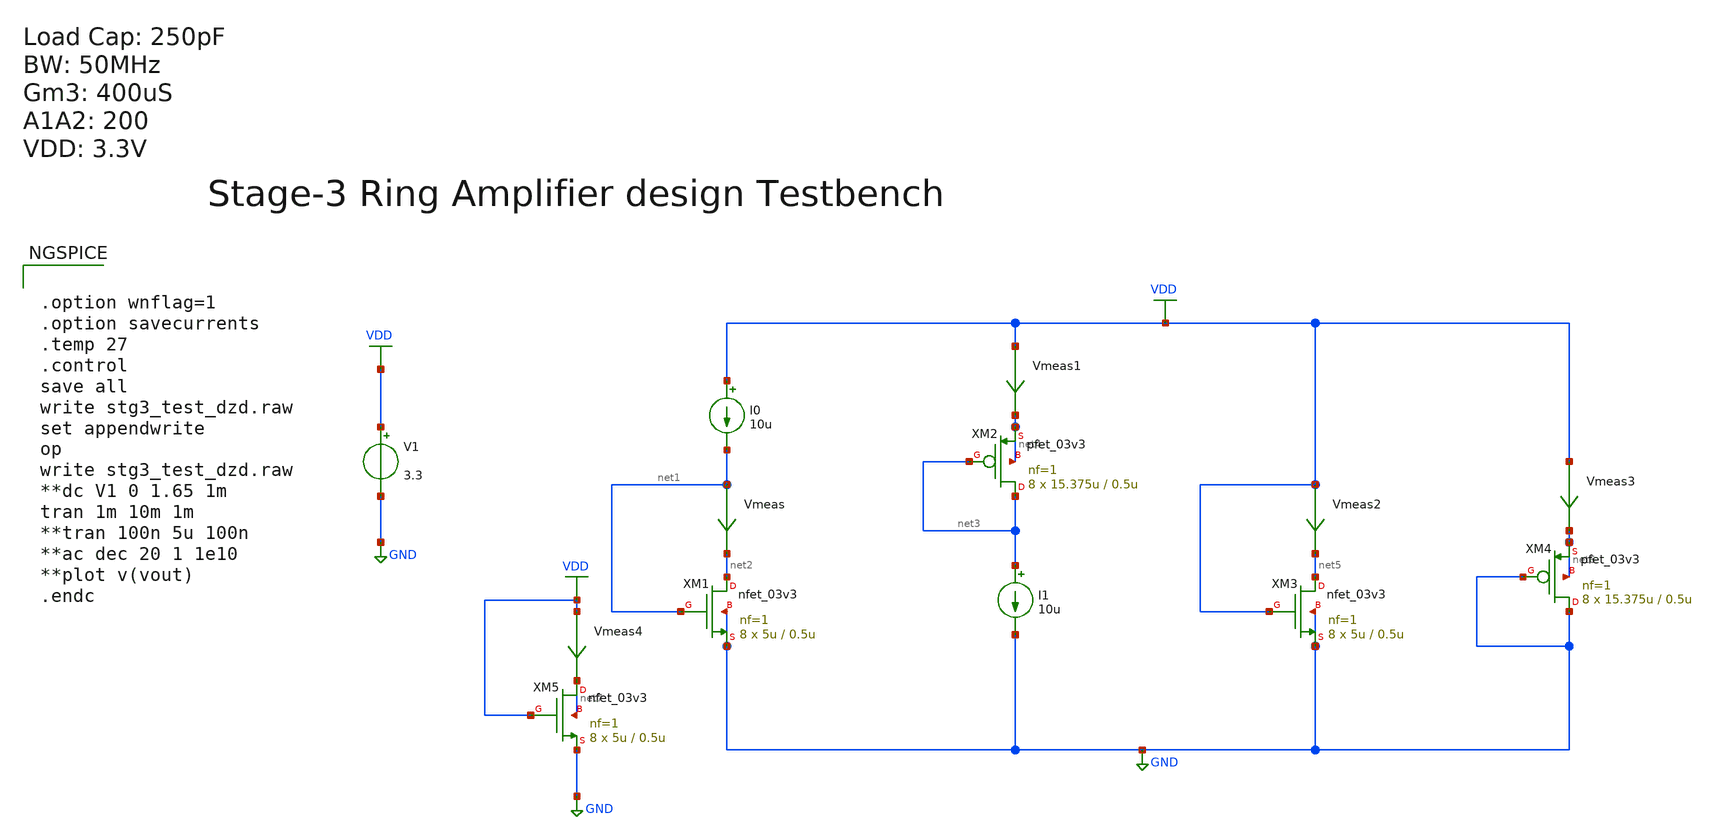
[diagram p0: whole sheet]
** sch_path: Design_Files/Ring-amp/STG3/stg3_test_dzd.sch
**.subckt stg3_test_dzd
XM1 net2 net1 GND GND nfet_03v3 L=0.5u W=5u nf=1 ad='int((nf+1)/2) * W/nf * 0.18u' as='int((nf+2)/2) * W/nf * 0.18u'
+ pd='2*int((nf+1)/2) * (W/nf + 0.18u)' ps='2*int((nf+2)/2) * (W/nf + 0.18u)' nrd='0.18u / W' nrs='0.18u / W'
+ sa=0 sb=0 sd=0 m=8
I0 VDD net1 10u
V1 VDD GND 3.3
Vmeas net1 net2 0
.save i(vmeas)
XM2 net3 net3 net4 net4 pfet_03v3 L=0.5u W=15.375u nf=1 ad='int((nf+1)/2) * W/nf * 0.18u' as='int((nf+2)/2) * W/nf * 0.18u'
+ pd='2*int((nf+1)/2) * (W/nf + 0.18u)' ps='2*int((nf+2)/2) * (W/nf + 0.18u)' nrd='0.18u / W' nrs='0.18u / W'
+ sa=0 sb=0 sd=0 m=8
I1 net3 GND 10u
Vmeas1 VDD net4 0
.save i(vmeas1)
XM3 net5 VDD GND GND nfet_03v3 L=0.5u W=5u nf=1 ad='int((nf+1)/2) * W/nf * 0.18u' as='int((nf+2)/2) * W/nf * 0.18u'
+ pd='2*int((nf+1)/2) * (W/nf + 0.18u)' ps='2*int((nf+2)/2) * (W/nf + 0.18u)' nrd='0.18u / W' nrs='0.18u / W'
+ sa=0 sb=0 sd=0 m=8
Vmeas2 VDD net5 0
.save i(vmeas2)
XM4 GND GND net6 net6 pfet_03v3 L=0.5u W=15.375u nf=1 ad='int((nf+1)/2) * W/nf * 0.18u' as='int((nf+2)/2) * W/nf * 0.18u'
+ pd='2*int((nf+1)/2) * (W/nf + 0.18u)' ps='2*int((nf+2)/2) * (W/nf + 0.18u)' nrd='0.18u / W' nrs='0.18u / W'
+ sa=0 sb=0 sd=0 m=8
Vmeas3 VDD net6 0
.save i(vmeas3)
XM5 net7 VDD GND net7 nfet_03v3 L=0.5u W=5u nf=1 ad='int((nf+1)/2) * W/nf * 0.18u' as='int((nf+2)/2) * W/nf * 0.18u'
+ pd='2*int((nf+1)/2) * (W/nf + 0.18u)' ps='2*int((nf+2)/2) * (W/nf + 0.18u)' nrd='0.18u / W' nrs='0.18u / W'
+ sa=0 sb=0 sd=0 m=8
Vmeas4 VDD net7 0
.save i(vmeas4)
**** begin user architecture code


.option wnflag=1
.option savecurrents
.temp 27
.control
save all
write stg3_test_dzd.raw
set appendwrite
op
write stg3_test_dzd.raw
**dc V1 0 1.65 1m
tran 1m 10m 1m
**tran 100n 5u 100n
**ac dec 20 1 1e10
**plot v(vout)
.endc




.lib /foss/pdks/volare/gf180mcu/versions/0fe599b2afb6708d281543108caf8310912f54af/gf180mcuD/libs.tech/ngspice/sm141064.ngspice typical
.include /foss/pdks/volare/gf180mcu/versions/0fe599b2afb6708d281543108caf8310912f54af/gf180mcuD/libs.tech/ngspice/design.ngspice

*.include $::180MCU_MODELS/design.ngspice
*.lib $::180MCU_MODELS/sm141064.ngspice typical




.save @m.xm1.m0[gm]
.save @m.xm1.m0[id]
.save @m.xm1.m0[vth]
.save @m.xm1.m0[gds]
.save @m.xm1.m0[cgg]
.save @m.xm1.m0[cgs]
.save @m.xm1.m0[cgd]
.save @m.xm2.m0[gm]
.save @m.xm2.m0[id]
.save @m.xm2.m0[vth]
.save @m.xm2.m0[gds]
.save @m.xm2.m0[cgg]
.save @m.xm2.m0[cgs]
.save @m.xm2.m0[cgd]
.save @m.xm3.m0[gm]
.save @m.xm3.m0[id]
.save @m.xm3.m0[vth]
.save @m.xm3.m0[vds]
.save @m.xm3.m0[gds]
.save @m.xm3.m0[cgg]
.save @m.xm3.m0[cgs]
.save @m.xm3.m0[cgd]
.save @m.xm4.m0[gm]
.save @m.xm4.m0[id]
.save @m.xm4.m0[vth]
.save @m.xm4.m0[vds]
.save @m.xm4.m0[gds]
.save @m.xm4.m0[cgg]
.save @m.xm4.m0[cgs]
.save @m.xm4.m0[cgd]


**** end user architecture code
**.ends
.GLOBAL GND
.GLOBAL VDD
.end
